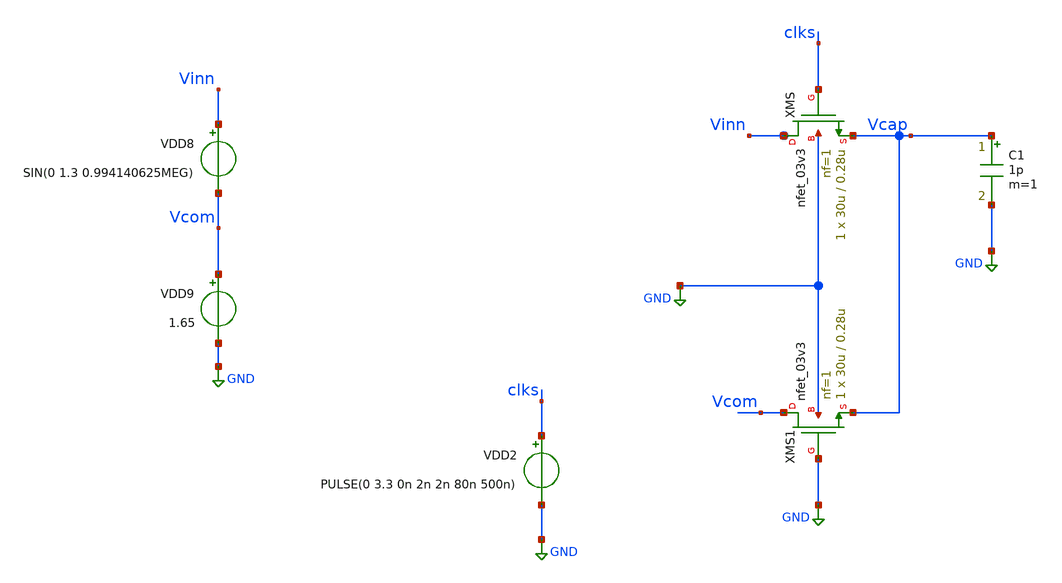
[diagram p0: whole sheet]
** sch_path: SAR_ADC/tracking_switches/xschem/switch_design_tb.sch
**.subckt switch_design_tb
XMS Vinn clks Vcap GND nfet_03v3 L=0.28u W=30u nf=1 ad='int((nf+1)/2) * W/nf * 0.18u' as='int((nf+2)/2) * W/nf * 0.18u'
+ pd='2*int((nf+1)/2) * (W/nf + 0.18u)' ps='2*int((nf+2)/2) * (W/nf + 0.18u)' nrd='0.18u / W' nrs='0.18u / W'
+ sa=0 sb=0 sd=0 m=1
VDD8 Vinn Vcom SIN(0 1.3 0.994140625MEG)
VDD9 Vcom GND 1.65
VDD2 clks GND PULSE(0 3.3 0n 2n 2n 80n 500n)
XMS1 Vcom GND Vcap GND nfet_03v3 L=0.28u W=30u nf=1 ad='int((nf+1)/2) * W/nf * 0.18u' as='int((nf+2)/2) * W/nf * 0.18u'
+ pd='2*int((nf+1)/2) * (W/nf + 0.18u)' ps='2*int((nf+2)/2) * (W/nf + 0.18u)' nrd='0.18u / W' nrs='0.18u / W'
+ sa=0 sb=0 sd=0 m=1
C1 Vcap GND 1p m=1
**** begin user architecture code



*Parameters

.options TEMP = 50.0
.lib /home/gf180/Documents/gf180/pdk/gf180mcuD/libs.tech/ngspice/sm141064.ngspice typical
.include /home/gf180/Documents/gf180/pdk/gf180mcuD/libs.tech/ngspice/design.ngspice
.lib /home/gf180/Documents/gf180/pdk/gf180mcuD/libs.tech/ngspice/sm141064.ngspice cap_mim
.lib /home/gf180/Documents/gf180/pdk/gf180mcuD/libs.tech/ngspice/sm141064.ngspice mimcap_statistical

*Data to save
.save all


* Simulation
.control
tran 1n 512u

*reset
*let start_w = 1u
*let delta_w = 2u
*let stop_w = 29u + delta_w/2.0
*let w_act = start_w
*while w_act le stop_w
* alterparam Wn = $w_act
* reset
plot V(Vcap)
* plot V(Vcap)
 save all
 set filetype = ascii
 write switch_design_tb_tran.raw
* let w_act = w_act + delta_w
* set appendwrite
*end

reset
unset filetype
op
save all
write switch_design_tb.raw


.endc
.end


**** end user architecture code
**.ends
.GLOBAL GND
.end
